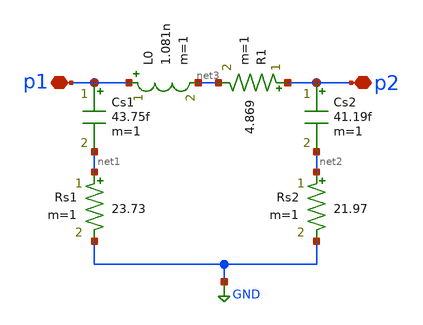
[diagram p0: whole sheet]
** sch_path: ask_modulator/xschem/l0.sch
**.subckt l0 p2 p1
*.iopin p2
*.iopin p1
L0 p1 net3 1.081n m=1
Cs1 p1 net1 43.75f m=1
Cs2 p2 net2 41.19f m=1
Rs1 net1 GND 23.73 m=1
Rs2 net2 GND 21.97 m=1
R1 p2 net3 4.869 m=1
**.ends
.GLOBAL GND
.end
